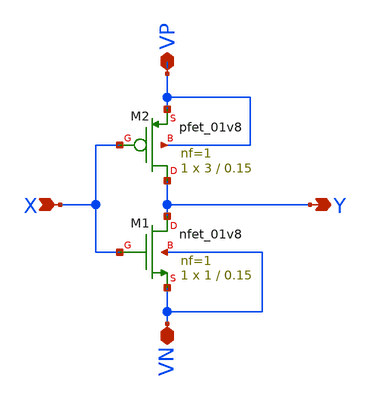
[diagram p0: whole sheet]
** sch_path: component/INV/INV_a.sch
**.subckt INV_a X Y VP VN
*.ipin X
*.opin Y
*.iopin VP
*.iopin VN
XM1 Y X VN VN sky130_fd_pr__nfet_01v8 L=0.15 W=1 nf=1 ad='int((nf+1)/2) * W/nf * 0.29' as='int((nf+2)/2) * W/nf * 0.29'
+ pd='2*int((nf+1)/2) * (W/nf + 0.29)' ps='2*int((nf+2)/2) * (W/nf + 0.29)' nrd='0.29 / W' nrs='0.29 / W'
+ sa=0 sb=0 sd=0 mult=1 m=1
XM2 Y X VP VP sky130_fd_pr__pfet_01v8 L=0.15 W=3 nf=1 ad='int((nf+1)/2) * W/nf * 0.29' as='int((nf+2)/2) * W/nf * 0.29'
+ pd='2*int((nf+1)/2) * (W/nf + 0.29)' ps='2*int((nf+2)/2) * (W/nf + 0.29)' nrd='0.29 / W' nrs='0.29 / W'
+ sa=0 sb=0 sd=0 mult=1 m=1
**.ends
.end
